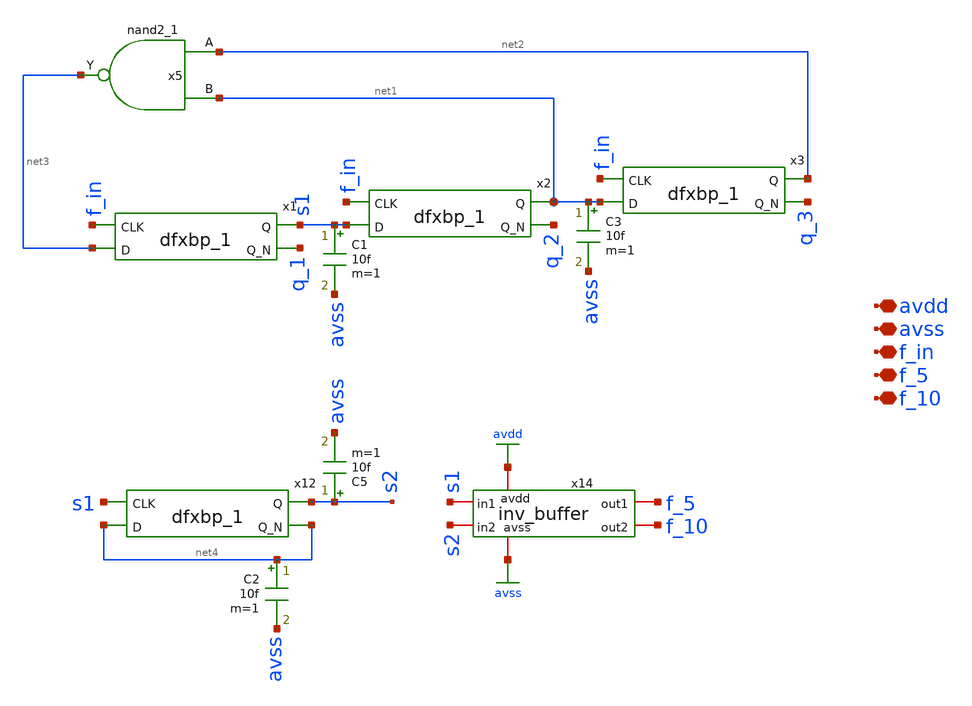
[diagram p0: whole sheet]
** sch_path: xschem/d_ff_10.sch
**.subckt d_ff_10 avdd avss f_in f_5 f_10
*.iopin avdd
*.iopin avss
*.iopin f_in
*.iopin f_5
*.iopin f_10
x1 f_in net3 VGND VNB VPB VPWR s1 q_1 sky130_fd_sc_hd__dfxbp_1
x2 f_in s1 VGND VNB VPB VPWR net1 q_2 sky130_fd_sc_hd__dfxbp_1
C1 s1 avss 10f m=1
x3 f_in net1 VGND VNB VPB VPWR net2 q_3 sky130_fd_sc_hd__dfxbp_1
x5 net2 net1 VGND VNB VPB VPWR net3 sky130_fd_sc_hd__nand2_1
C3 net1 avss 10f m=1
x12 s1 net4 VGND VNB VPB VPWR s2 net4 sky130_fd_sc_hd__dfxbp_1
C2 net4 avss 10f m=1
C5 s2 avss 10f m=1
x14 avdd avss f_5 f_10 s2 s1 inv_buffer
**.ends
.GLOBAL avdd
.GLOBAL avss
.end
